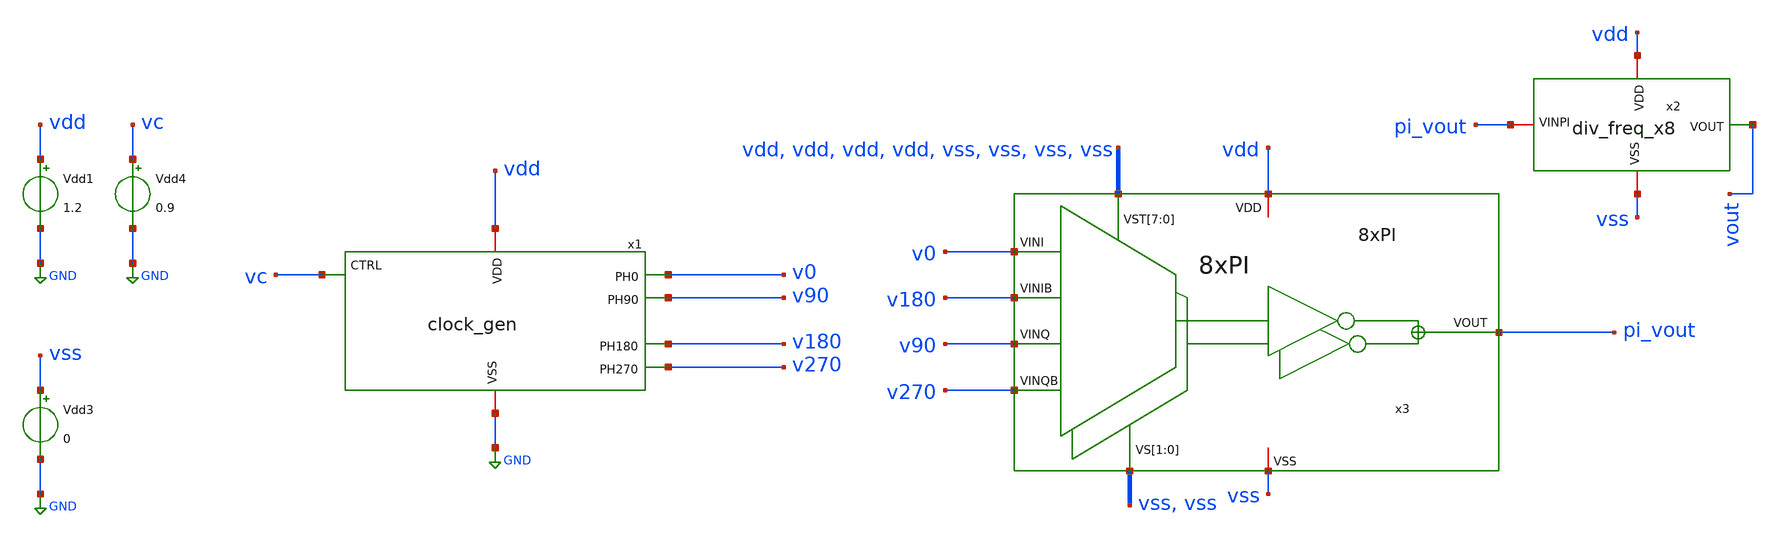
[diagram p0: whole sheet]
** sch_path: Clock_Gen/tb_2to4.sch
**.subckt tb_2to4
Vdd1 vdd GND 1.2
Vdd4 vc GND 0.9
x3 v0 v180 v90 v270 vss vss vdd vdd vdd vdd vss vss vss vss pi_vout vdd vss 8xPI
Vdd3 vss GND 0
x1 v0 v90 vdd vc v180 GND v270 clock_gen
x2 vdd pi_vout vout vss div_freq_x8
**** begin user architecture code


.save v(vin1) v(v0) v(v90) v(v270) v(v180) v(vin2) v(vout) v(pi_vout)


.tran 5p 16n
.save all

.control
run
set color0=white
write tran_logic.raw

* --- MEDICIONES DE FASE Y RETARDO (Usando v90) ---
* Periodo Entrada (Ref)
*meas tran T_p90 TRIG v(vin1) VAL=0.6 RISE=3 TARG v(vin1) VAL=0.6 RISE=4

* Retardo (Entrada vs v90)
*meas tran T_d90 TRIG v(vin1) VAL=0.6 RISE=3 TARG v(v90) VAL=0.6 RISE=3

* Calculo Fase
*let Phase_D90= (T_d90 / T_p90) * 360

*print T_p90
*print T_d90
*print Phase_D90


* --- DUTY CYCLE (Usando v90) ---
* Periodo Salida
*meas tran T_pe90 TRIG v(v90) VAL=0.6 RISE=2 TARG v(v90) VAL=0.6 RISE=3

* Tiempo en ALTO (Ton)
* Desde que sube (RISE=2) hasta que baja (FALL=2)
*meas tran T_h90 TRIG v(v90) VAL=0.6 RISE=2 TARG v(v90) VAL=0.6 FALL=2

* Tiempo en BAJO (Toff)
* Desde que baja (FALL=2) hasta que sube de nuevo (RISE=3)
*meas tran T_l90 TRIG v(v90) VAL=0.6 FALL=2 TARG v(v90) VAL=0.6 RISE=3

*let Duty_H90 = (T_h90 / T_pe90) * 100
*let Duty_L90 = (T_l90 / T_pe90) * 100

*print Duty_H90
*print Duty_L90

meas tran SKEW0_90 TRIG v(v0) VAL=0.6 RISE=3 TARG v(v90) VAL=0.6 RISE=4
meas tran SKEW90_180 TRIG v(v90) VAL=0.6 RISE=3 TARG v(v180) VAL=0.6 RISE=3
meas tran SKEW180_270 TRIG v(v180) VAL=0.6 RISE=3 TARG v(v270) VAL=0.6 RISE=4
meas tran SKEW270_0 TRIG v(v270) VAL=0.6 RISE=4 TARG v(v0) VAL=0.6 RISE=3

meas tran T90 TRIG v(v90) VAL=0.6 RISE=3 TARG v(v90) VAL=0.6 RISE=4
meas tran T180 TRIG v(v180) VAL=0.6 RISE=3 TARG v(v180) VAL=0.6 RISE=4
meas tran T270 TRIG v(v270) VAL=0.6 RISE=3 TARG v(v270) VAL=0.6 RISE=4
meas tran T0 TRIG v(v0) VAL=0.6 RISE=3 TARG v(v0) VAL=0.6 RISE=4

let period_0 = T0
let period_90 = T90
let period_180 = T180
let period_270 = T270

let phase0_90 = (SKEW0_90 / period_0) * 360
let phase90_180 = (SKEW90_180 / period_0) * 360
let phase180_270 = (SKEW180_270 / period_0) * 360
let phase270_0 = (SKEW270_0 / period_0) * 360


meas tran PW0 TRIG v(v0) VAL=0.6 RISE=3 TARG v(v0) VAL=0.6 FALL=4
meas tran PW90 TRIG v(v90) VAL=0.6 RISE=3 TARG v(v90) VAL=0.6 FALL=4
meas tran PW180 TRIG v(v180) VAL=0.6 RISE=3 TARG v(v180) VAL=0.6 FALL=3
meas tran PW270 TRIG v(v270) VAL=0.6 RISE=3 TARG v(v270) VAL=0.6 FALL=3

let Duty0 = PW0 / period_0
let Duty90 = PW90 / period_90
let Duty180 = PW180 / period_180
let Duty270 = PW270 / period_270


let freq = 1 / period_0

print SKEW0_90 SKEW90_180 SKEW180_270 SKEW270_0 phase0_90 phase90_180 phase180_270 phase270_0 PW0
+ PW90 PW180 PW270 Duty0 Duty90 Duty180 Duty270 freq

.endc



.lib cornerMOSlv.lib mos_tt
*.include /foss/pdks/ihp-sg13g2/libs.ref/sg13g2_stdcell/spice/sg13g2_stdcell.spice


**** end user architecture code
**.ends
.GLOBAL GND
.end
